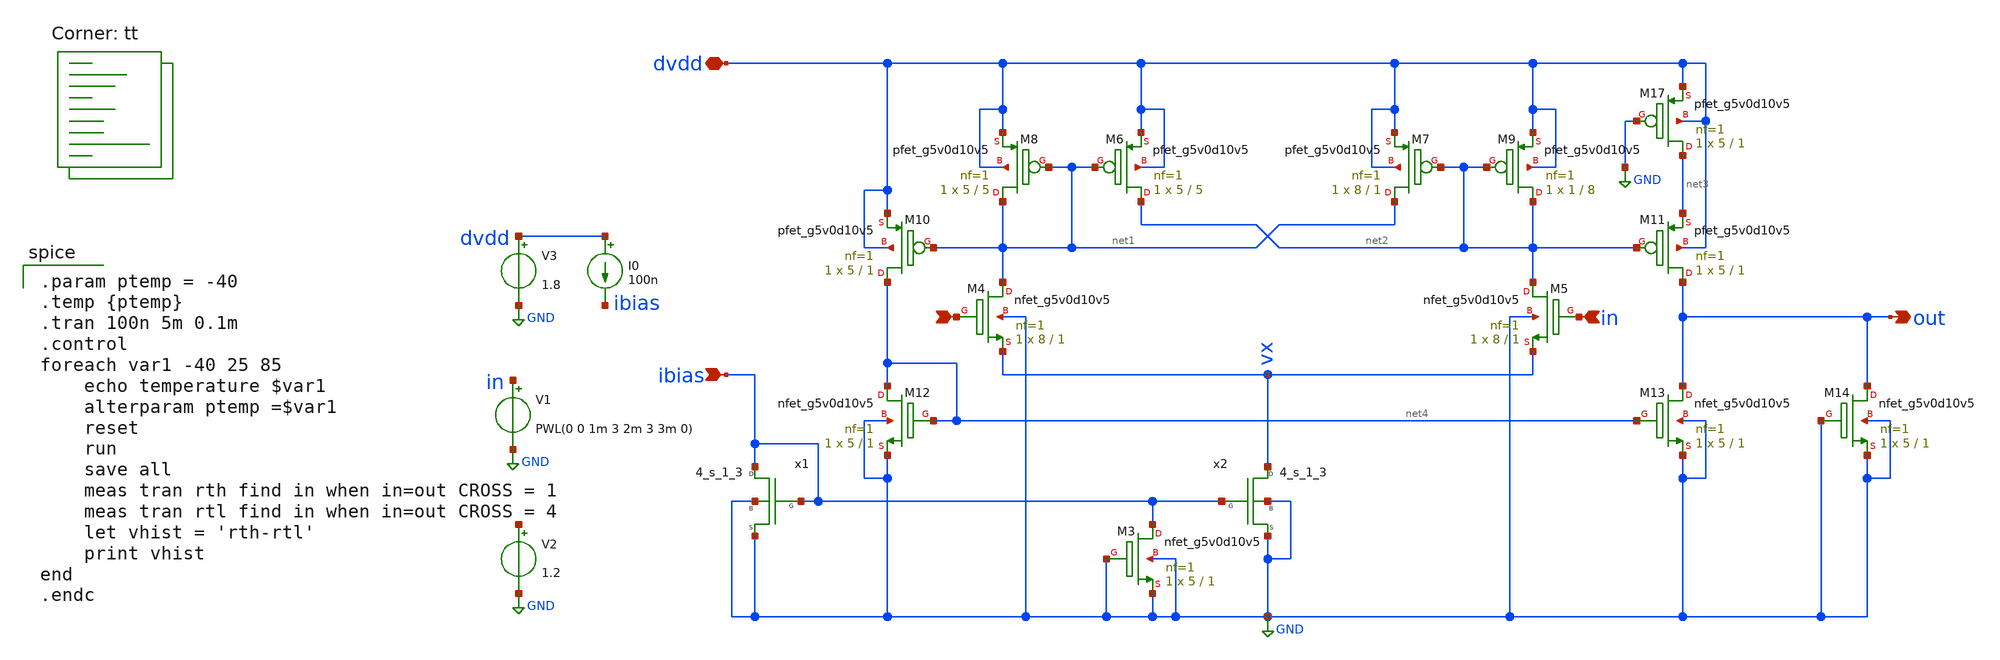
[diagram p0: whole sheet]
** sch_path: xschem_final/Comparador_histerese_mod.sch
**.subckt Comparador_histerese_mod dvdd ibias - in out
*.iopin dvdd
*.ipin ibias
*.ipin -
*.ipin in
*.opin out
XM17 net3 GND dvdd dvdd sky130_fd_pr__pfet_g5v0d10v5 L=1 W=5 nf=1 ad='int((nf+1)/2) * W/nf * 0.29' as='int((nf+2)/2) * W/nf * 0.29'
+ pd='2*int((nf+1)/2) * (W/nf + 0.29)' ps='2*int((nf+2)/2) * (W/nf + 0.29)' nrd='0.29 / W' nrs='0.29 / W'
+ sa=0 sb=0 sd=0 mult=1 m=1
XM3 ibias GND GND GND sky130_fd_pr__nfet_g5v0d10v5 L=1 W=5 nf=1 ad='int((nf+1)/2) * W/nf * 0.29' as='int((nf+2)/2) * W/nf * 0.29'
+ pd='2*int((nf+1)/2) * (W/nf + 0.29)' ps='2*int((nf+2)/2) * (W/nf + 0.29)' nrd='0.29 / W' nrs='0.29 / W'
+ sa=0 sb=0 sd=0 mult=1 m=1
XM4 net1 - vx GND sky130_fd_pr__nfet_g5v0d10v5 L=1 W=8 nf=1 ad='int((nf+1)/2) * W/nf * 0.29' as='int((nf+2)/2) * W/nf * 0.29'
+ pd='2*int((nf+1)/2) * (W/nf + 0.29)' ps='2*int((nf+2)/2) * (W/nf + 0.29)' nrd='0.29 / W' nrs='0.29 / W'
+ sa=0 sb=0 sd=0 mult=1 m=1
XM5 net2 in vx GND sky130_fd_pr__nfet_g5v0d10v5 L=1 W=8 nf=1 ad='int((nf+1)/2) * W/nf * 0.29' as='int((nf+2)/2) * W/nf * 0.29'
+ pd='2*int((nf+1)/2) * (W/nf + 0.29)' ps='2*int((nf+2)/2) * (W/nf + 0.29)' nrd='0.29 / W' nrs='0.29 / W'
+ sa=0 sb=0 sd=0 mult=1 m=1
XM6 net2 net1 dvdd dvdd sky130_fd_pr__pfet_g5v0d10v5 L=5 W=5 nf=1 ad='int((nf+1)/2) * W/nf * 0.29' as='int((nf+2)/2) * W/nf * 0.29'
+ pd='2*int((nf+1)/2) * (W/nf + 0.29)' ps='2*int((nf+2)/2) * (W/nf + 0.29)' nrd='0.29 / W' nrs='0.29 / W'
+ sa=0 sb=0 sd=0 mult=1 m=1
XM7 net1 net2 dvdd dvdd sky130_fd_pr__pfet_g5v0d10v5 L=1 W=8 nf=1 ad='int((nf+1)/2) * W/nf * 0.29' as='int((nf+2)/2) * W/nf * 0.29'
+ pd='2*int((nf+1)/2) * (W/nf + 0.29)' ps='2*int((nf+2)/2) * (W/nf + 0.29)' nrd='0.29 / W' nrs='0.29 / W'
+ sa=0 sb=0 sd=0 mult=1 m=1
XM8 net1 net1 dvdd dvdd sky130_fd_pr__pfet_g5v0d10v5 L=5 W=5 nf=1 ad='int((nf+1)/2) * W/nf * 0.29' as='int((nf+2)/2) * W/nf * 0.29'
+ pd='2*int((nf+1)/2) * (W/nf + 0.29)' ps='2*int((nf+2)/2) * (W/nf + 0.29)' nrd='0.29 / W' nrs='0.29 / W'
+ sa=0 sb=0 sd=0 mult=1 m=1
XM9 net2 net2 dvdd dvdd sky130_fd_pr__pfet_g5v0d10v5 L=8 W=1 nf=1 ad='int((nf+1)/2) * W/nf * 0.29' as='int((nf+2)/2) * W/nf * 0.29'
+ pd='2*int((nf+1)/2) * (W/nf + 0.29)' ps='2*int((nf+2)/2) * (W/nf + 0.29)' nrd='0.29 / W' nrs='0.29 / W'
+ sa=0 sb=0 sd=0 mult=1 m=1
XM10 net4 net1 dvdd dvdd sky130_fd_pr__pfet_g5v0d10v5 L=1 W=5 nf=1 ad='int((nf+1)/2) * W/nf * 0.29' as='int((nf+2)/2) * W/nf * 0.29'
+ pd='2*int((nf+1)/2) * (W/nf + 0.29)' ps='2*int((nf+2)/2) * (W/nf + 0.29)' nrd='0.29 / W' nrs='0.29 / W'
+ sa=0 sb=0 sd=0 mult=1 m=1
XM11 out net2 net3 dvdd sky130_fd_pr__pfet_g5v0d10v5 L=1 W=5 nf=1 ad='int((nf+1)/2) * W/nf * 0.29' as='int((nf+2)/2) * W/nf * 0.29'
+ pd='2*int((nf+1)/2) * (W/nf + 0.29)' ps='2*int((nf+2)/2) * (W/nf + 0.29)' nrd='0.29 / W' nrs='0.29 / W'
+ sa=0 sb=0 sd=0 mult=1 m=1
XM12 net4 net4 GND GND sky130_fd_pr__nfet_g5v0d10v5 L=1 W=5 nf=1 ad='int((nf+1)/2) * W/nf * 0.29' as='int((nf+2)/2) * W/nf * 0.29'
+ pd='2*int((nf+1)/2) * (W/nf + 0.29)' ps='2*int((nf+2)/2) * (W/nf + 0.29)' nrd='0.29 / W' nrs='0.29 / W'
+ sa=0 sb=0 sd=0 mult=1 m=1
XM13 out net4 GND GND sky130_fd_pr__nfet_g5v0d10v5 L=1 W=5 nf=1 ad='int((nf+1)/2) * W/nf * 0.29' as='int((nf+2)/2) * W/nf * 0.29'
+ pd='2*int((nf+1)/2) * (W/nf + 0.29)' ps='2*int((nf+2)/2) * (W/nf + 0.29)' nrd='0.29 / W' nrs='0.29 / W'
+ sa=0 sb=0 sd=0 mult=1 m=1
XM14 out GND GND GND sky130_fd_pr__nfet_g5v0d10v5 L=1 W=5 nf=1 ad='int((nf+1)/2) * W/nf * 0.29' as='int((nf+2)/2) * W/nf * 0.29'
+ pd='2*int((nf+1)/2) * (W/nf + 0.29)' ps='2*int((nf+2)/2) * (W/nf + 0.29)' nrd='0.29 / W' nrs='0.29 / W'
+ sa=0 sb=0 sd=0 mult=1 m=1
V1 in GND PWL(0 0 1m 3 2m 3 3m 0)
V2 - GND 1.2
V3 dvdd GND 1.8
I0 dvdd ibias 100n
x1 ibias GND ibias GND 4_s_1_3
x2 vx GND ibias GND 4_s_1_3
**** begin user architecture code
.lib $::SKYWATER_MODELS/sky130.lib.spice tt

.param ptemp = -40
.temp {ptemp}
.tran 100n 5m 0.1m
.control
foreach var1 -40 25 85
	echo temperature $var1
	alterparam ptemp =$var1
	reset
	run
	save all
	meas tran rth find in when in=out CROSS = 1
	meas tran rtl find in when in=out CROSS = 4
	let vhist = 'rth-rtl'
	print vhist
end
.endc

**** end user architecture code
**.ends
.GLOBAL GND
.end
